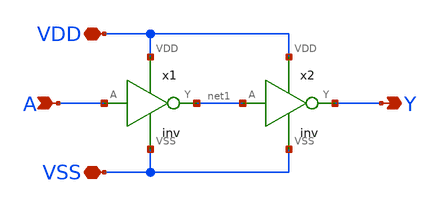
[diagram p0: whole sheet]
** sch_path: examples/buffer/libs/logic/buf/schematic/buf.sch
**.subckt buf A Y VDD VSS
*.ipin A
*.opin Y
*.iopin VDD
*.iopin VSS
x1 A net1 VDD VSS inv
x2 net1 Y VDD VSS inv
**.ends
.end
